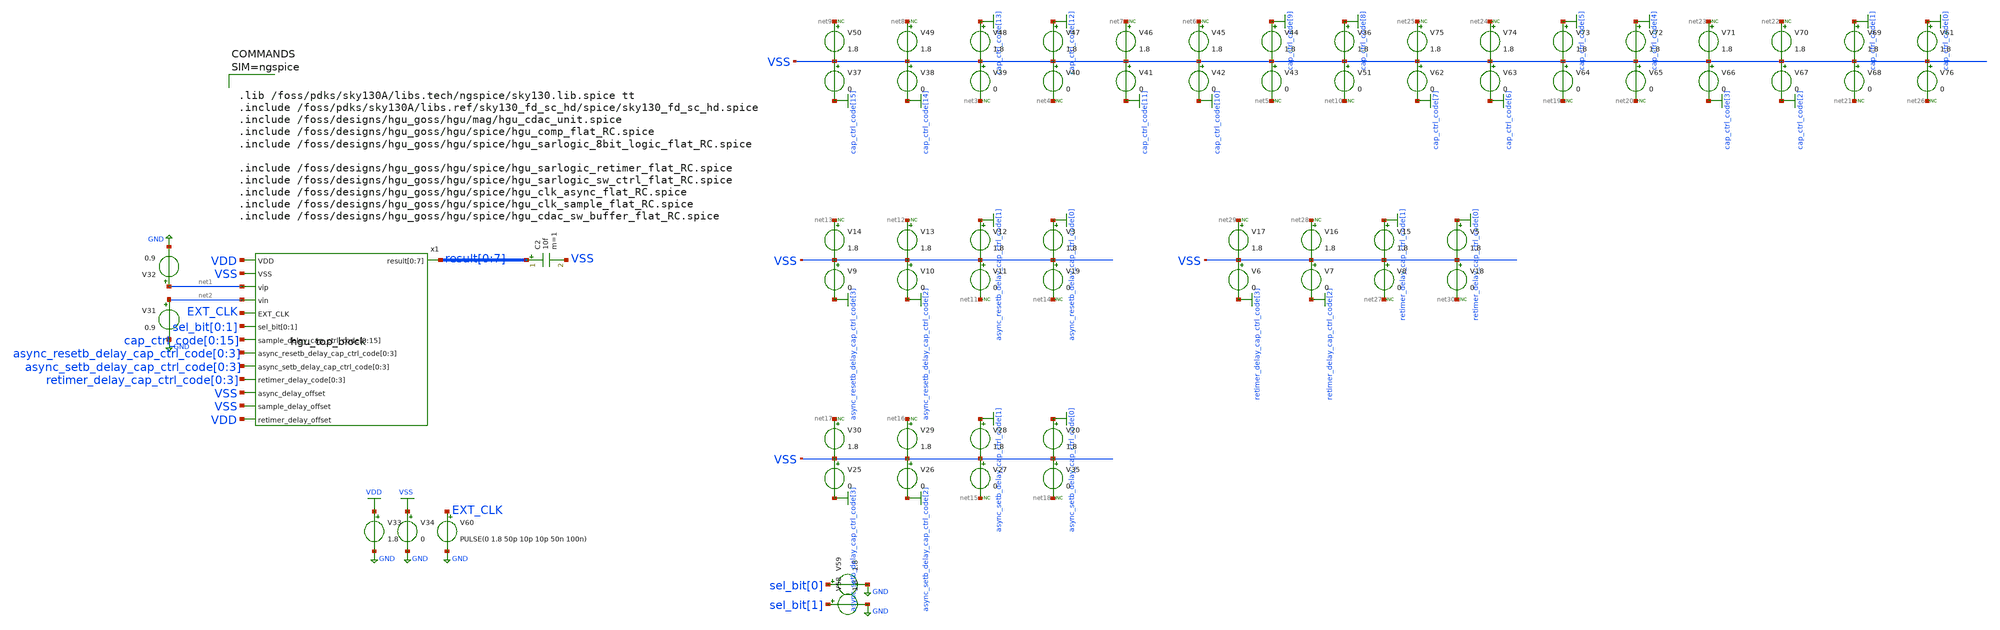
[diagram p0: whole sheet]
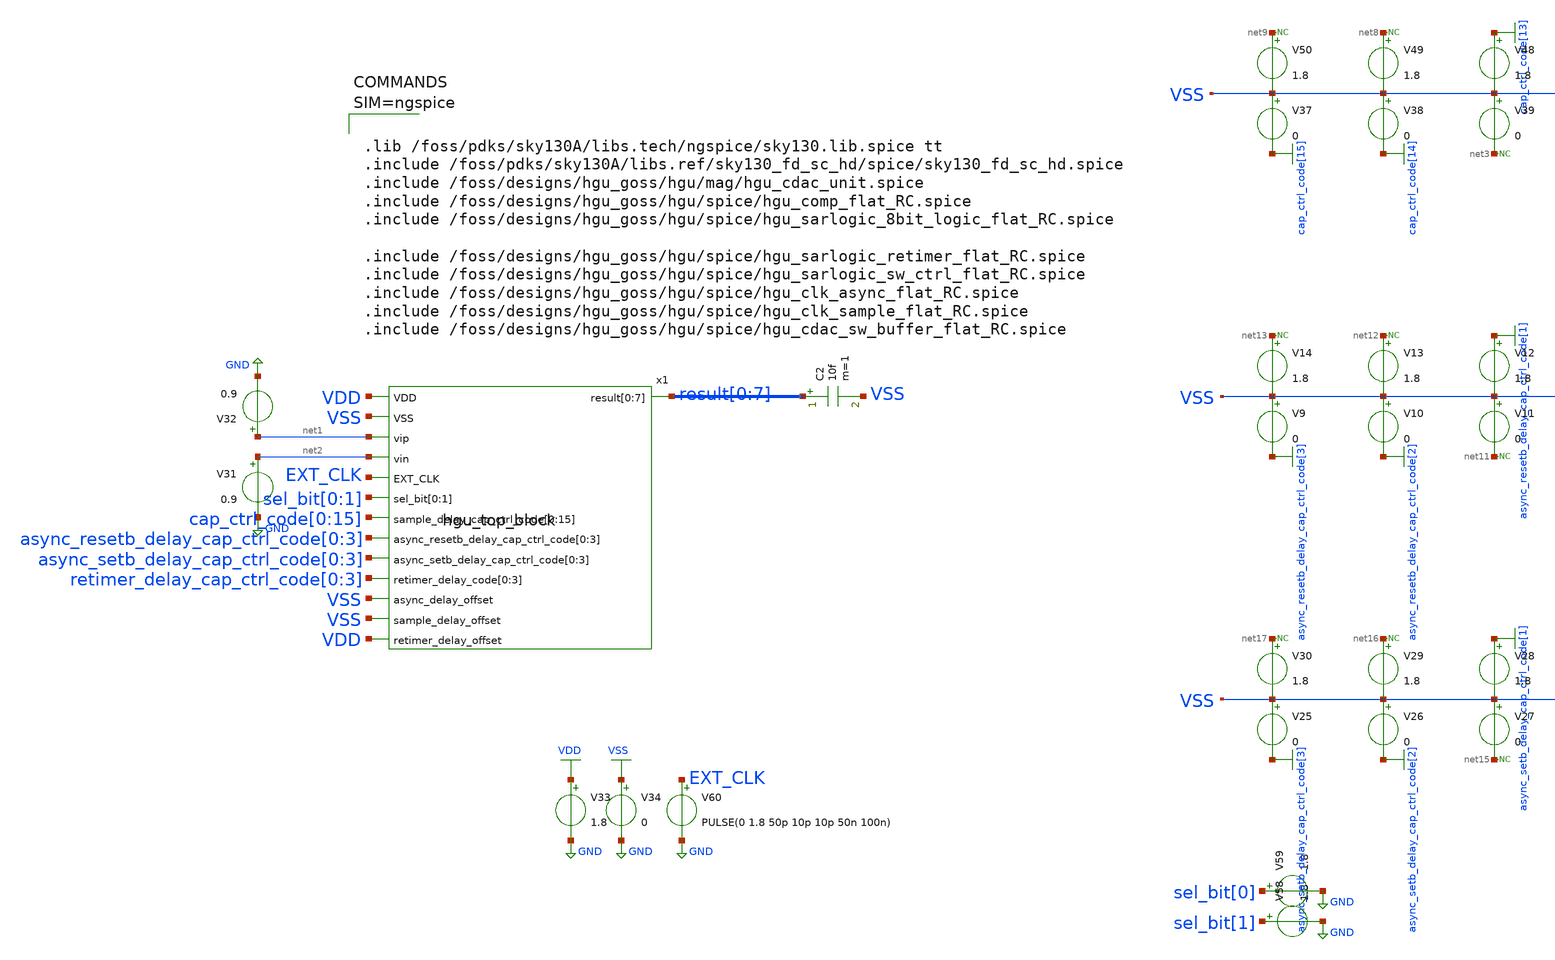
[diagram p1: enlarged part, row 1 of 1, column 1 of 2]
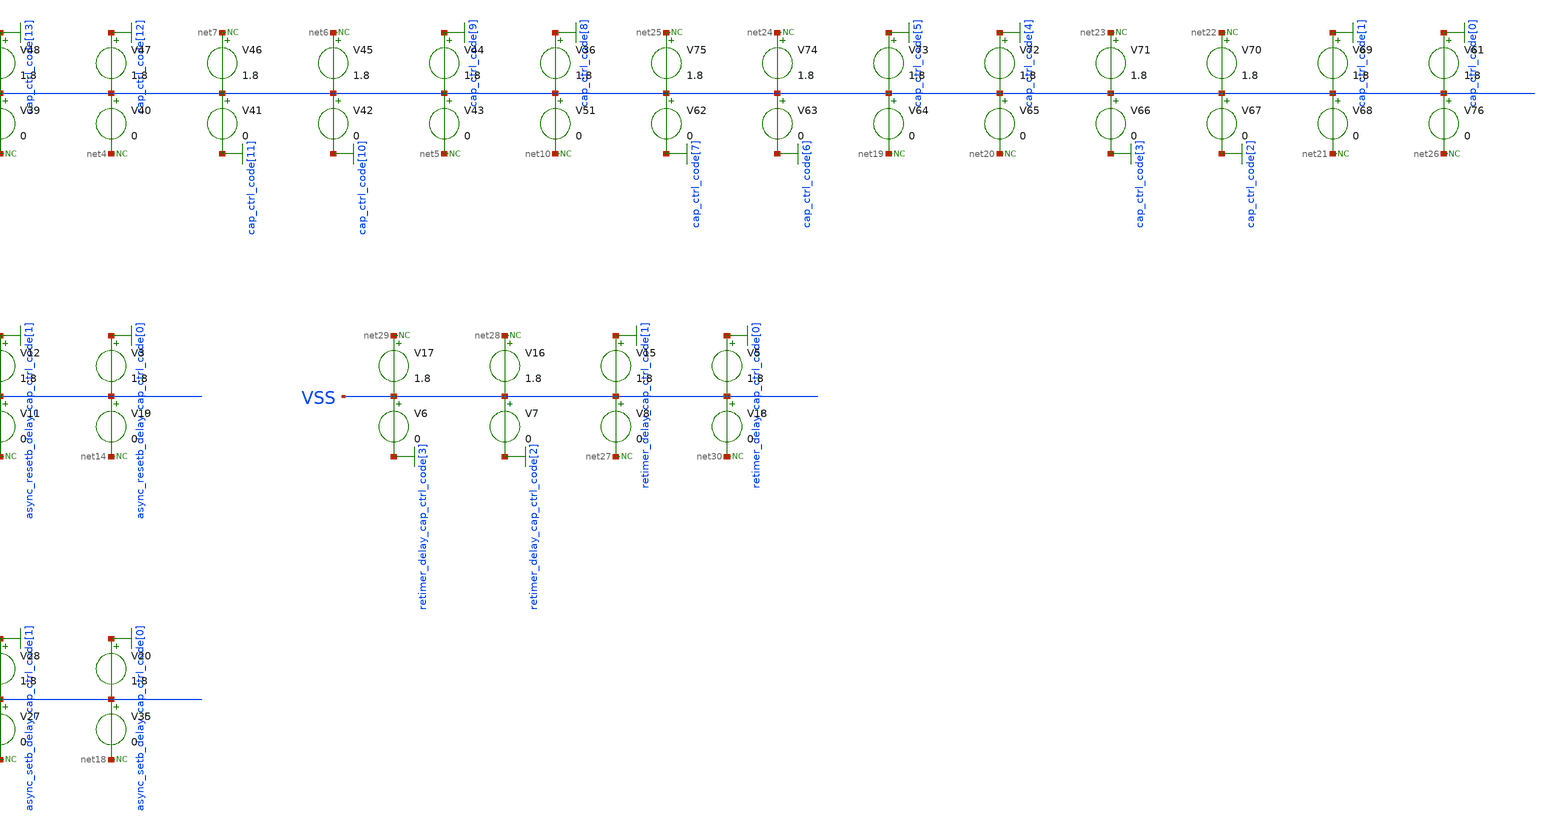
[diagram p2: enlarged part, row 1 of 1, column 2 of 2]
** sch_path: hgu/tb/tb_hgu_top_block.sch
**.subckt tb_hgu_top_block
x1 VDD result[0] result[1] result[2] result[3] result[4] result[5] result[6] result[7] VSS net1 net2
+ EXT_CLK sel_bit[0] sel_bit[1] cap_ctrl_code[0] cap_ctrl_code[1] cap_ctrl_code[2] cap_ctrl_code[3]
+ cap_ctrl_code[4] cap_ctrl_code[5] cap_ctrl_code[6] cap_ctrl_code[7] cap_ctrl_code[8] cap_ctrl_code[9]
+ cap_ctrl_code[10] cap_ctrl_code[11] cap_ctrl_code[12] cap_ctrl_code[13] cap_ctrl_code[14] cap_ctrl_code[15]
+ async_resetb_delay_cap_ctrl_code[0] async_resetb_delay_cap_ctrl_code[1] async_resetb_delay_cap_ctrl_code[2]
+ async_resetb_delay_cap_ctrl_code[3] async_setb_delay_cap_ctrl_code[0] async_setb_delay_cap_ctrl_code[1]
+ async_setb_delay_cap_ctrl_code[2] async_setb_delay_cap_ctrl_code[3] retimer_delay_cap_ctrl_code[0] retimer_delay_cap_ctrl_code[1]
+ retimer_delay_cap_ctrl_code[2] retimer_delay_cap_ctrl_code[3] VSS VSS VDD hgu_top_block
C2 result[0] VSS 10f m=1
V36 cap_ctrl_code[8] VSS 1.8
V37 VSS cap_ctrl_code[15] 0
V38 VSS cap_ctrl_code[14] 0
V39 VSS net3 0
V40 VSS net4 0
V41 VSS cap_ctrl_code[11] 0
V42 VSS cap_ctrl_code[10] 0
V43 VSS net5 0
V44 cap_ctrl_code[9] VSS 1.8
V45 net6 VSS 1.8
V46 net7 VSS 1.8
V47 cap_ctrl_code[12] VSS 1.8
V48 cap_ctrl_code[13] VSS 1.8
V49 net8 VSS 1.8
V50 net9 VSS 1.8
V51 VSS net10 0
* noconn #net9
* noconn #net8
* noconn #net3
* noconn #net4
* noconn #net7
* noconn #net6
* noconn #net5
* noconn #net10
V58 sel_bit[1] GND 1.8
V59 sel_bit[0] GND 1.8
V3 async_resetb_delay_cap_ctrl_code[0] VSS 1.8
V9 VSS async_resetb_delay_cap_ctrl_code[3] 0
V10 VSS async_resetb_delay_cap_ctrl_code[2] 0
V11 VSS net11 0
V12 async_resetb_delay_cap_ctrl_code[1] VSS 1.8
V13 net12 VSS 1.8
V14 net13 VSS 1.8
V19 VSS net14 0
* noconn #net13
* noconn #net12
* noconn #net11
* noconn #net14
V20 async_setb_delay_cap_ctrl_code[0] VSS 1.8
V25 VSS async_setb_delay_cap_ctrl_code[3] 0
V26 VSS async_setb_delay_cap_ctrl_code[2] 0
V27 VSS net15 0
V28 async_setb_delay_cap_ctrl_code[1] VSS 1.8
V29 net16 VSS 1.8
V30 net17 VSS 1.8
V35 VSS net18 0
* noconn #net17
* noconn #net16
* noconn #net15
* noconn #net18
V61 cap_ctrl_code[0] VSS 1.8
V62 VSS cap_ctrl_code[7] 0
V63 VSS cap_ctrl_code[6] 0
V64 VSS net19 0
V65 VSS net20 0
V66 VSS cap_ctrl_code[3] 0
V67 VSS cap_ctrl_code[2] 0
V68 VSS net21 0
V69 cap_ctrl_code[1] VSS 1.8
V70 net22 VSS 1.8
V71 net23 VSS 1.8
V72 cap_ctrl_code[4] VSS 1.8
V73 cap_ctrl_code[5] VSS 1.8
V74 net24 VSS 1.8
V75 net25 VSS 1.8
V76 VSS net26 0
* noconn #net25
* noconn #net24
* noconn #net19
* noconn #net20
* noconn #net23
* noconn #net22
* noconn #net21
* noconn #net26
V5 retimer_delay_cap_ctrl_code[0] VSS 1.8
V6 VSS retimer_delay_cap_ctrl_code[3] 0
V7 VSS retimer_delay_cap_ctrl_code[2] 0
V8 VSS net27 0
V15 retimer_delay_cap_ctrl_code[1] VSS 1.8
V16 net28 VSS 1.8
V17 net29 VSS 1.8
V18 VSS net30 0
* noconn #net29
* noconn #net28
* noconn #net27
* noconn #net30
V33 VDD GND 1.8
V34 VSS GND 0
V31 net2 GND 0.9
V32 net1 GND 0.9
V60 EXT_CLK GND PULSE(0 1.8 50p 10p 10p 50n 100n)
**** begin user architecture code



.lib /foss/pdks/sky130A/libs.tech/ngspice/sky130.lib.spice tt
.include /foss/pdks/sky130A/libs.ref/sky130_fd_sc_hd/spice/sky130_fd_sc_hd.spice
.include /foss/designs/hgu_goss/hgu/mag/hgu_cdac_unit.spice
.include /foss/designs/hgu_goss/hgu/spice/hgu_comp_flat_RC.spice
.include /foss/designs/hgu_goss/hgu/spice/hgu_sarlogic_8bit_logic_flat_RC.spice

.include /foss/designs/hgu_goss/hgu/spice/hgu_sarlogic_retimer_flat_RC.spice
.include /foss/designs/hgu_goss/hgu/spice/hgu_sarlogic_sw_ctrl_flat_RC.spice
.include /foss/designs/hgu_goss/hgu/spice/hgu_clk_async_flat_RC.spice
.include /foss/designs/hgu_goss/hgu/spice/hgu_clk_sample_flat_RC.spice
.include /foss/designs/hgu_goss/hgu/spice/hgu_cdac_sw_buffer_flat_RC.spice






.OPTIONS savecurrents
.tran 10ps 250ns

.control
	run
	plot V(sample_clk) V(vip) V(vin) V(vip)-V(vin)+0.9 V(tah_vp) V(tah_vn) V(tah_vp)-V(tah_vn)
+ V(vip)-V(vin)


.endc
.save sample_clk vip vin tah_vp tah_vn "result[0]" "result[1]" "result[2]" "result[3]" "result[4]" "result[5]" "result[6]" "result[7]"



**** end user architecture code
**.ends
.GLOBAL cap_ctrl_code[15]
.GLOBAL cap_ctrl_code[14]
.GLOBAL cap_ctrl_code[13]
.GLOBAL cap_ctrl_code[12]
.GLOBAL cap_ctrl_code[11]
.GLOBAL cap_ctrl_code[10]
.GLOBAL cap_ctrl_code[9]
.GLOBAL cap_ctrl_code[8]
.GLOBAL GND
.GLOBAL async_resetb_delay_cap_ctrl_code[3]
.GLOBAL async_resetb_delay_cap_ctrl_code[2]
.GLOBAL async_resetb_delay_cap_ctrl_code[1]
.GLOBAL async_resetb_delay_cap_ctrl_code[0]
.GLOBAL async_setb_delay_cap_ctrl_code[3]
.GLOBAL async_setb_delay_cap_ctrl_code[2]
.GLOBAL async_setb_delay_cap_ctrl_code[1]
.GLOBAL async_setb_delay_cap_ctrl_code[0]
.GLOBAL cap_ctrl_code[7]
.GLOBAL cap_ctrl_code[6]
.GLOBAL cap_ctrl_code[5]
.GLOBAL cap_ctrl_code[4]
.GLOBAL cap_ctrl_code[3]
.GLOBAL cap_ctrl_code[2]
.GLOBAL cap_ctrl_code[1]
.GLOBAL cap_ctrl_code[0]
.GLOBAL retimer_delay_cap_ctrl_code[3]
.GLOBAL retimer_delay_cap_ctrl_code[2]
.GLOBAL retimer_delay_cap_ctrl_code[1]
.GLOBAL retimer_delay_cap_ctrl_code[0]
.GLOBAL VDD
.GLOBAL VSS
.end
